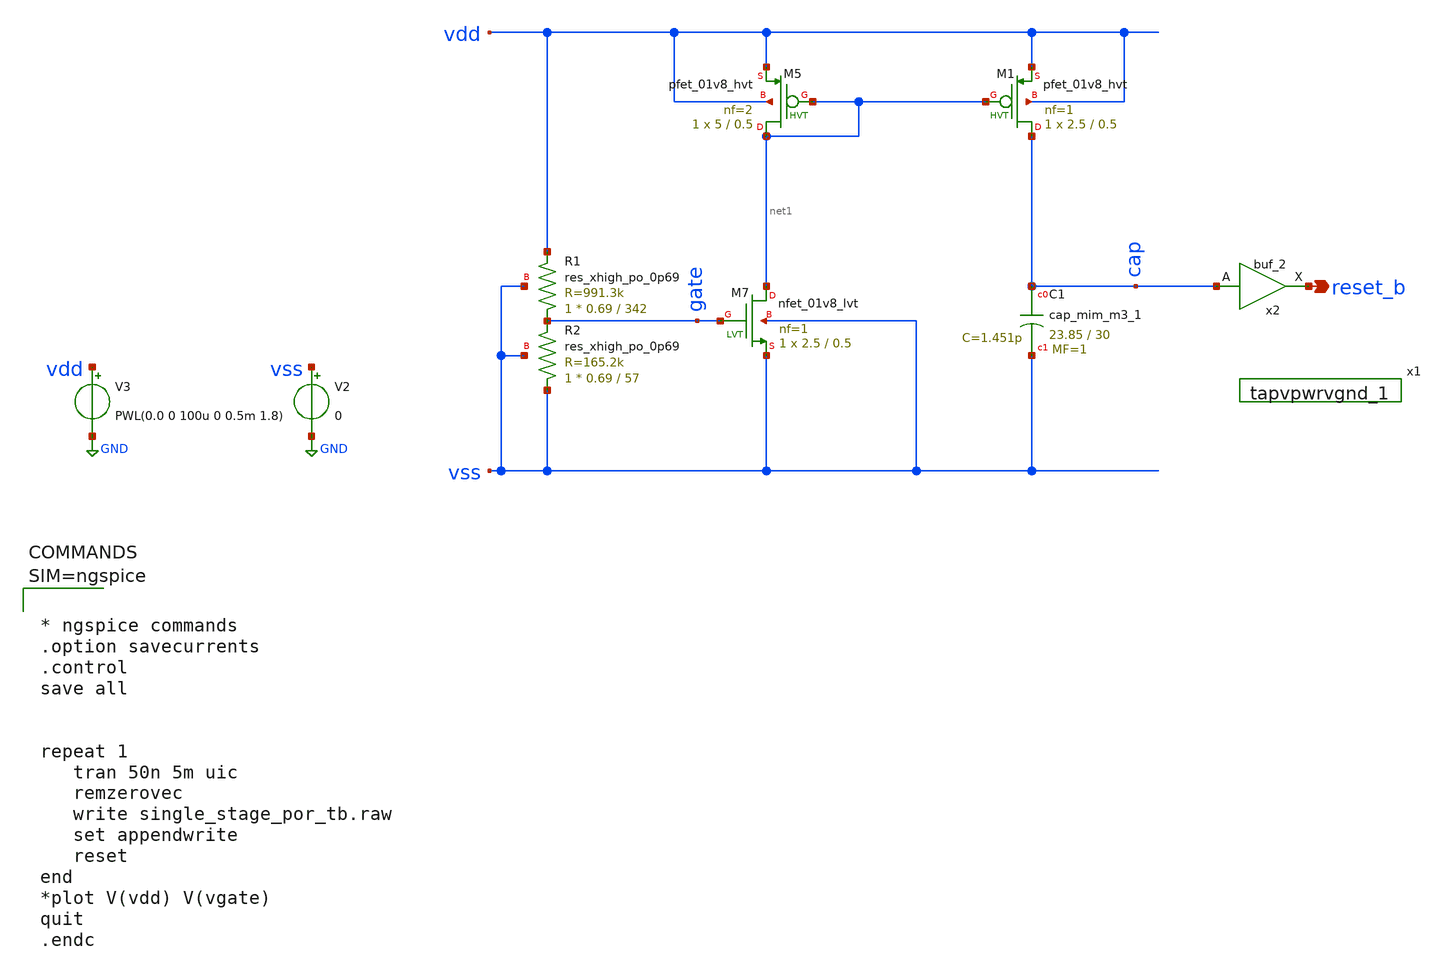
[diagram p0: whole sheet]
** sch_path: xschem/single_stage_por_tb.sch
**.subckt single_stage_por_tb reset_b
*.opin reset_b
V2 vss GND 0
XM5 net1 net1 vdd vdd sky130_fd_pr__pfet_01v8_hvt L=0.5 W=5 nf=2 ad='int((nf+1)/2) * W/nf * 0.29' as='int((nf+2)/2) * W/nf * 0.29'
+ pd='2*int((nf+1)/2) * (W/nf + 0.29)' ps='2*int((nf+2)/2) * (W/nf + 0.29)' nrd='0.29 / W' nrs='0.29 / W'
+ sa=0 sb=0 sd=0 mult=1 m=1
XM7 net1 gate vss vss sky130_fd_pr__nfet_01v8_lvt L=0.5 W=2.5 nf=1 ad='int((nf+1)/2) * W/nf * 0.29' as='int((nf+2)/2) * W/nf * 0.29'
+ pd='2*int((nf+1)/2) * (W/nf + 0.29)' ps='2*int((nf+2)/2) * (W/nf + 0.29)' nrd='0.29 / W' nrs='0.29 / W'
+ sa=0 sb=0 sd=0 mult=1 m=1
V3 vdd GND PWL(0.0 0 100u 0 0.5m 1.8)
XR1 gate vdd vss sky130_fd_pr__res_xhigh_po_0p69 L=342 mult=1 m=1
XR2 vss gate vss sky130_fd_pr__res_xhigh_po_0p69 L=57 mult=1 m=1
XM1 cap net1 vdd vdd sky130_fd_pr__pfet_01v8_hvt L=0.5 W=2.5 nf=1 ad='int((nf+1)/2) * W/nf * 0.29' as='int((nf+2)/2) * W/nf * 0.29'
+ pd='2*int((nf+1)/2) * (W/nf + 0.29)' ps='2*int((nf+2)/2) * (W/nf + 0.29)' nrd='0.29 / W' nrs='0.29 / W'
+ sa=0 sb=0 sd=0 mult=1 m=1
XC1 cap vss sky130_fd_pr__cap_mim_m3_1 W=23.85 L=30 MF=1 m=1
x2 cap VSS VSS VDD VDD reset_b sky130_fd_sc_hd__buf_2
x1 vss vdd sky130_fd_sc_hd__tapvpwrvgnd_1
**** begin user architecture code

** opencircuitdesign pdks install
.lib $::SKYWATER_MODELS/sky130.lib.spice tt
.include $::SKYWATER_STDCELLS/sky130_fd_sc_hd.spice
.temp 27




* ngspice commands
.option savecurrents
.control
save all


repeat 1
   tran 50n 5m uic
   remzerovec
   write single_stage_por_tb.raw
   set appendwrite
   reset
end
*plot V(vdd) V(vgate)
quit
.endc



**** end user architecture code
**.ends
.GLOBAL GND
.end
